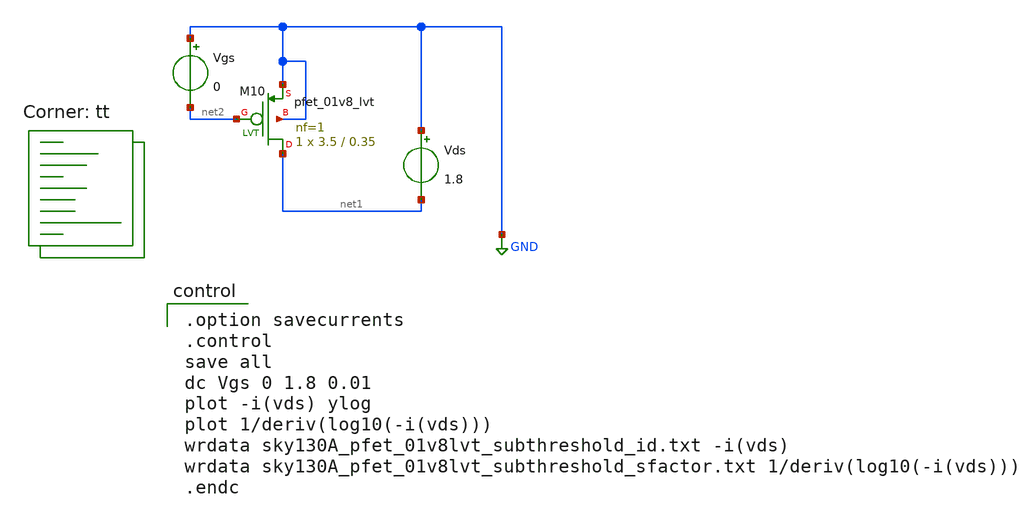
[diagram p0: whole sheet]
** sch_path: xschem/MOSFET/sky130A_pfet_01v8lvt_subthreshold.sch
**.subckt sky130A_pfet_01v8lvt_subthreshold
Vgs GND net2 0
Vds GND net1 1.8
XM10 net1 net2 GND GND sky130_fd_pr__pfet_01v8_lvt L=0.35 W=3.5 nf=1 ad='int((1 + 1)/2) * 3.5 / 1 * 0.29'
+ as='int((1 + 2)/2) * 3.5 / 1 * 0.29' pd='2*int((1 + 1)/2) * (3.5 / 1 + 0.29)' ps='2*int((1 + 2)/2) * (3.5 / 1 + 0.29)'
+ nrd='0.29 / 3.5 ' nrs='0.29 / 3.5 ' sa=0 sb=0 sd=0 mult=1 m=1
**** begin user architecture code

.option savecurrents
.control
save all
dc Vgs 0 1.8 0.01
plot -i(vds) ylog
plot 1/deriv(log10(-i(vds)))
wrdata sky130A_pfet_01v8lvt_subthreshold_id.txt -i(vds)
wrdata sky130A_pfet_01v8lvt_subthreshold_sfactor.txt 1/deriv(log10(-i(vds)))
.endc

.lib $::SKYWATER_MODELS/sky130.lib.spice tt
**** end user architecture code
**.ends
.GLOBAL GND
.end
